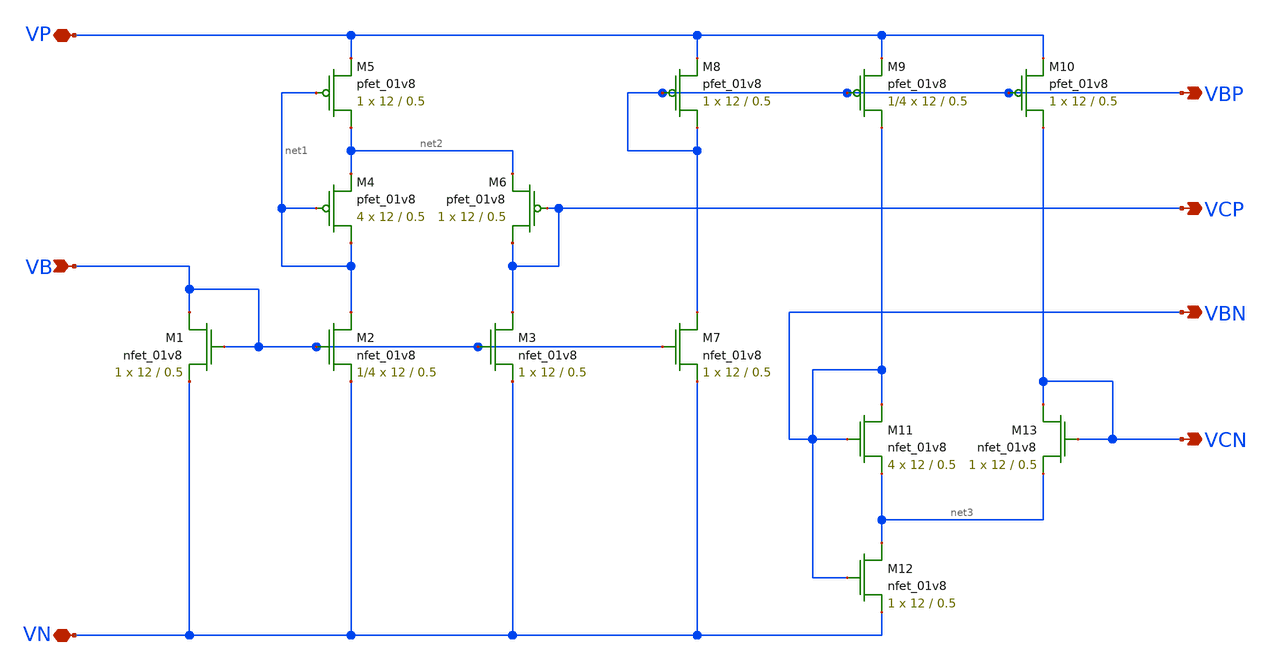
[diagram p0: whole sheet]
** sch_path: mp3/bias_gen/bias_gen.sch
**.subckt bias_gen VN VP VCN VCP VBP VB VBN
*.iopin VN
*.iopin VP
*.opin VCN
*.opin VCP
*.opin VBP
*.ipin VB
*.opin VBN
XM1 VB VB VN VN sky130_fd_pr__nfet_01v8 L=0.5 W=12 nf=1 ad='int((nf+1)/2) * W/nf * 0.29' as='int((nf+2)/2) * W/nf * 0.29'
+ pd='2*int((nf+1)/2) * (W/nf + 0.29)' ps='2*int((nf+2)/2) * (W/nf + 0.29)' nrd='0.29 / W' nrs='0.29 / W'
+ sa=0 sb=0 sd=0 mult=1 m=1
XM2 net1 VB VN VN sky130_fd_pr__nfet_01v8 L=0.5 W=12 nf=1 ad='int((nf+1)/2) * W/nf * 0.29' as='int((nf+2)/2) * W/nf * 0.29'
+ pd='2*int((nf+1)/2) * (W/nf + 0.29)' ps='2*int((nf+2)/2) * (W/nf + 0.29)' nrd='0.29 / W' nrs='0.29 / W'
+ sa=0 sb=0 sd=0 mult=1/4 m=1/4
XM3 VCP VB VN VN sky130_fd_pr__nfet_01v8 L=0.5 W=12 nf=1 ad='int((nf+1)/2) * W/nf * 0.29' as='int((nf+2)/2) * W/nf * 0.29'
+ pd='2*int((nf+1)/2) * (W/nf + 0.29)' ps='2*int((nf+2)/2) * (W/nf + 0.29)' nrd='0.29 / W' nrs='0.29 / W'
+ sa=0 sb=0 sd=0 mult=1 m=1
XM4 net1 net1 net2 VP sky130_fd_pr__pfet_01v8 L=0.5 W=12 nf=1 ad='int((nf+1)/2) * W/nf * 0.29' as='int((nf+2)/2) * W/nf * 0.29'
+ pd='2*int((nf+1)/2) * (W/nf + 0.29)' ps='2*int((nf+2)/2) * (W/nf + 0.29)' nrd='0.29 / W' nrs='0.29 / W'
+ sa=0 sb=0 sd=0 mult=4 m=4
XM5 net2 net1 VP VP sky130_fd_pr__pfet_01v8 L=0.5 W=12 nf=1 ad='int((nf+1)/2) * W/nf * 0.29' as='int((nf+2)/2) * W/nf * 0.29'
+ pd='2*int((nf+1)/2) * (W/nf + 0.29)' ps='2*int((nf+2)/2) * (W/nf + 0.29)' nrd='0.29 / W' nrs='0.29 / W'
+ sa=0 sb=0 sd=0 mult=1 m=1
XM6 VCP VCP net2 VP sky130_fd_pr__pfet_01v8 L=0.5 W=12 nf=1 ad='int((nf+1)/2) * W/nf * 0.29' as='int((nf+2)/2) * W/nf * 0.29'
+ pd='2*int((nf+1)/2) * (W/nf + 0.29)' ps='2*int((nf+2)/2) * (W/nf + 0.29)' nrd='0.29 / W' nrs='0.29 / W'
+ sa=0 sb=0 sd=0 mult=1 m=1
XM7 VBP VB VN VN sky130_fd_pr__nfet_01v8 L=0.5 W=12 nf=1 ad='int((nf+1)/2) * W/nf * 0.29' as='int((nf+2)/2) * W/nf * 0.29'
+ pd='2*int((nf+1)/2) * (W/nf + 0.29)' ps='2*int((nf+2)/2) * (W/nf + 0.29)' nrd='0.29 / W' nrs='0.29 / W'
+ sa=0 sb=0 sd=0 mult=1 m=1
XM8 VBP VBP VP VP sky130_fd_pr__pfet_01v8 L=0.5 W=12 nf=1 ad='int((nf+1)/2) * W/nf * 0.29' as='int((nf+2)/2) * W/nf * 0.29'
+ pd='2*int((nf+1)/2) * (W/nf + 0.29)' ps='2*int((nf+2)/2) * (W/nf + 0.29)' nrd='0.29 / W' nrs='0.29 / W'
+ sa=0 sb=0 sd=0 mult=1 m=1
XM9 VBN VBP VP VP sky130_fd_pr__pfet_01v8 L=0.5 W=12 nf=1 ad='int((nf+1)/2) * W/nf * 0.29' as='int((nf+2)/2) * W/nf * 0.29'
+ pd='2*int((nf+1)/2) * (W/nf + 0.29)' ps='2*int((nf+2)/2) * (W/nf + 0.29)' nrd='0.29 / W' nrs='0.29 / W'
+ sa=0 sb=0 sd=0 mult=1/4 m=1/4
XM10 VCN VBP VP VP sky130_fd_pr__pfet_01v8 L=0.5 W=12 nf=1 ad='int((nf+1)/2) * W/nf * 0.29' as='int((nf+2)/2) * W/nf * 0.29'
+ pd='2*int((nf+1)/2) * (W/nf + 0.29)' ps='2*int((nf+2)/2) * (W/nf + 0.29)' nrd='0.29 / W' nrs='0.29 / W'
+ sa=0 sb=0 sd=0 mult=1 m=1
XM11 VBN VBN net3 VN sky130_fd_pr__nfet_01v8 L=0.5 W=12 nf=1 ad='int((nf+1)/2) * W/nf * 0.29' as='int((nf+2)/2) * W/nf * 0.29'
+ pd='2*int((nf+1)/2) * (W/nf + 0.29)' ps='2*int((nf+2)/2) * (W/nf + 0.29)' nrd='0.29 / W' nrs='0.29 / W'
+ sa=0 sb=0 sd=0 mult=4 m=4
XM12 net3 VBN VN VN sky130_fd_pr__nfet_01v8 L=0.5 W=12 nf=1 ad='int((nf+1)/2) * W/nf * 0.29' as='int((nf+2)/2) * W/nf * 0.29'
+ pd='2*int((nf+1)/2) * (W/nf + 0.29)' ps='2*int((nf+2)/2) * (W/nf + 0.29)' nrd='0.29 / W' nrs='0.29 / W'
+ sa=0 sb=0 sd=0 mult=1 m=1
XM13 VCN VCN net3 VN sky130_fd_pr__nfet_01v8 L=0.5 W=12 nf=1 ad='int((nf+1)/2) * W/nf * 0.29' as='int((nf+2)/2) * W/nf * 0.29'
+ pd='2*int((nf+1)/2) * (W/nf + 0.29)' ps='2*int((nf+2)/2) * (W/nf + 0.29)' nrd='0.29 / W' nrs='0.29 / W'
+ sa=0 sb=0 sd=0 mult=1 m=1
**.ends
.end
